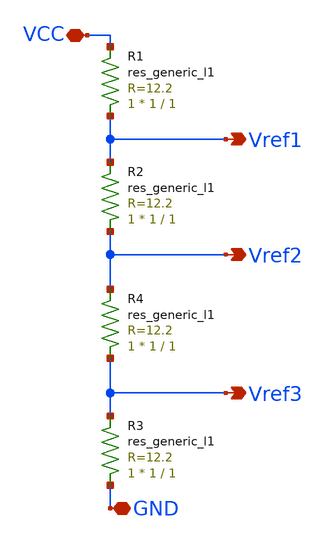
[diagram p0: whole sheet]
** sch_path: week7/pre-layout/rbridge.sch
**.subckt rbridge GND Vref1 Vref2 Vref3 VCC
*.iopin GND
*.opin Vref1
*.opin Vref2
*.opin Vref3
*.iopin VCC
R1 Vref1 VCC sky130_fd_pr__res_generic_l1 W=1 L=1 m=1
R2 Vref2 Vref1 sky130_fd_pr__res_generic_l1 W=1 L=1 m=1
R3 GND Vref3 sky130_fd_pr__res_generic_l1 W=1 L=1 m=1
R4 Vref3 Vref2 sky130_fd_pr__res_generic_l1 W=1 L=1 m=1
**.ends
.end
